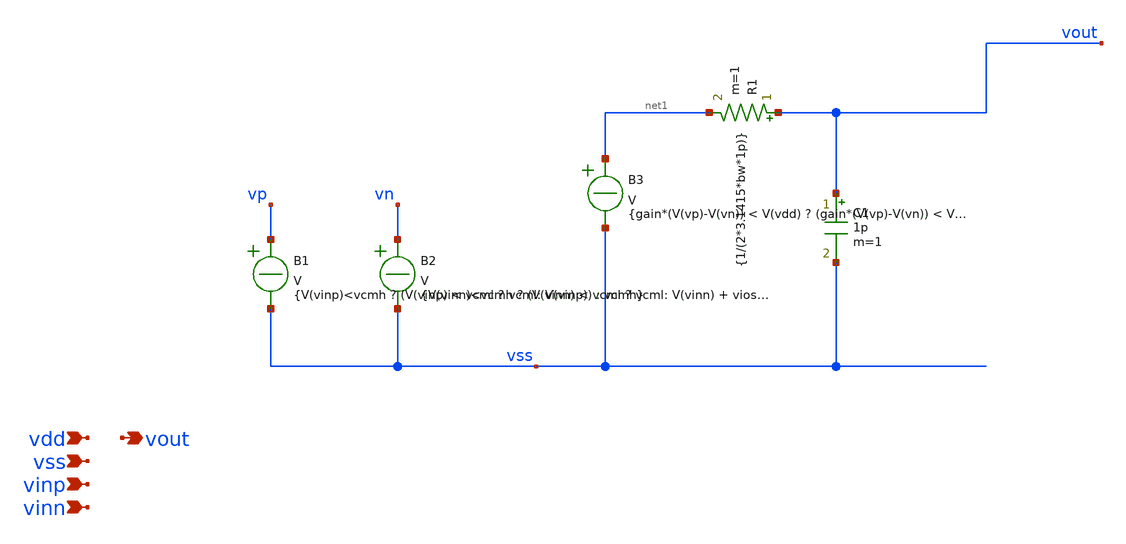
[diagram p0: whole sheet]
** sch_path: schematics/ideal_comp.sch
**.subckt ideal_comp vdd vout vss vinp vinn
*.ipin vdd
*.opin vout
*.ipin vss
*.ipin vinp
*.ipin vinn
B1 vp vss V = {V(vinp)<vcmh ? (V(vinp) < vcml ? vcml: V(vinp)) : vcmh}
B2 vn vss V = {V(vinn)<vcmh ? (V(vinn) < vcml ? vcml: V(vinn) + vios) : vcmh}
B3 net1 vss V = {gain*(V(vp)-V(vn)) < V(vdd) ? (gain*(V(vp)-V(vn)) < V(vss) ? V(vss) : (gain*(V(vp)-V(vn)))) : V(vdd)}
R1 vout net1 {1/(2*3.1415*bw*1p)} m=1
C1 vout vss 1p m=1
**.ends
.end
